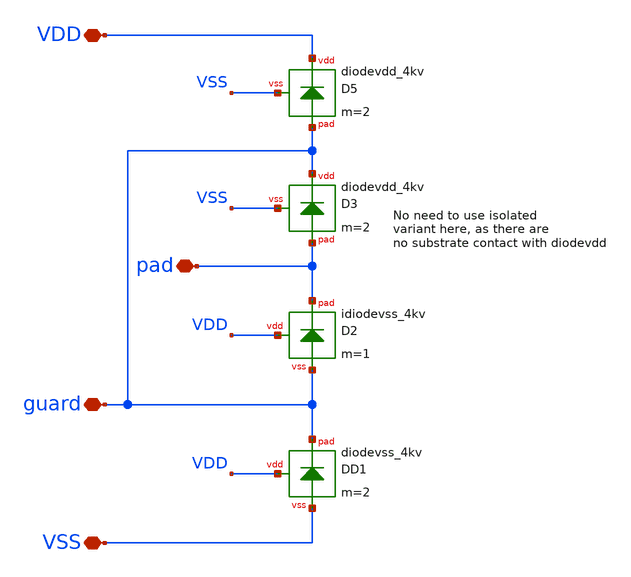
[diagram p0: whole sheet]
** sch_path: trident_test_structures/design_data/xschem/IOPadAnalogGuardLayer/first_stage_diodes_4kv_guard_layer.sch
**.subckt first_stage_diodes_4kv_guard_layer VSS VDD pad guard
*.iopin VSS
*.iopin VDD
*.iopin pad
*.iopin guard
XD5 VDD guard VSS diodevdd_4kv m=2
XD3 guard pad VSS diodevdd_4kv m=2
XD1 VDD guard VSS diodevss_4kv m=2
XD2 VDD pad guard idiodevss_4kv m=1
**.ends
.end
